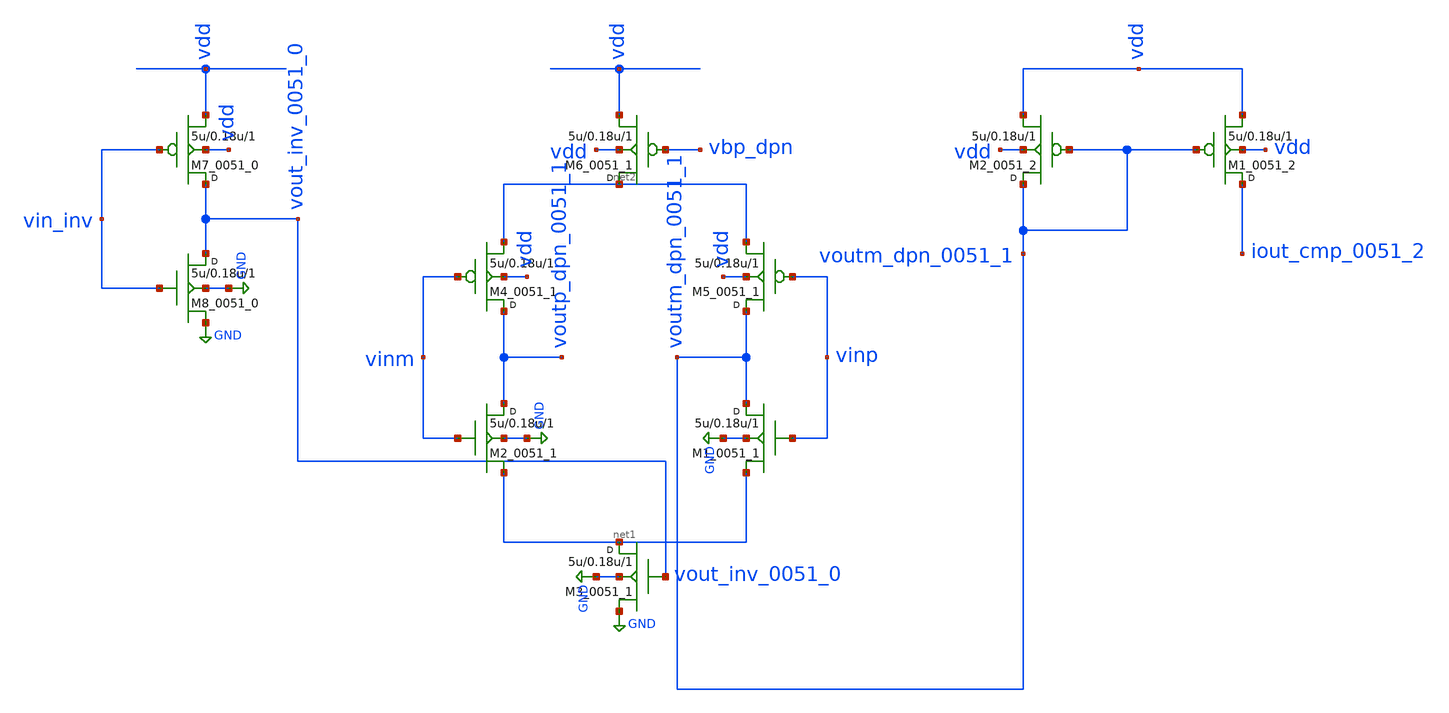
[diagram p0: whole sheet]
** sch_path: synthetic/generated/0051_generated.sch
**.subckt 0051_generated
M7_0051_0 vout_inv_0051_0 vin_inv vdd vdd pmos w=5u l=0.18u m=1
M8_0051_0 vout_inv_0051_0 vin_inv GND GND nmos w=5u l=0.18u m=1
M1_0051_1 voutm_dpn_0051_1 vinp net1 GND nmos w=5u l=0.18u m=1
M2_0051_1 voutp_dpn_0051_1 vinm net1 GND nmos w=5u l=0.18u m=1
M3_0051_1 net1 vout_inv_0051_0 GND GND nmos w=5u l=0.18u m=1
M4_0051_1 voutp_dpn_0051_1 vinm net2 vdd pmos w=5u l=0.18u m=1
M5_0051_1 voutm_dpn_0051_1 vinp net2 vdd pmos w=5u l=0.18u m=1
M6_0051_1 net2 vbp_dpn vdd vdd pmos w=5u l=0.18u m=1
M1_0051_2 iout_cmp_0051_2 voutm_dpn_0051_1 vdd vdd pmos w=5u l=0.18u m=1
M2_0051_2 voutm_dpn_0051_1 voutm_dpn_0051_1 vdd vdd pmos w=5u l=0.18u m=1
**.ends
.GLOBAL GND
.end
